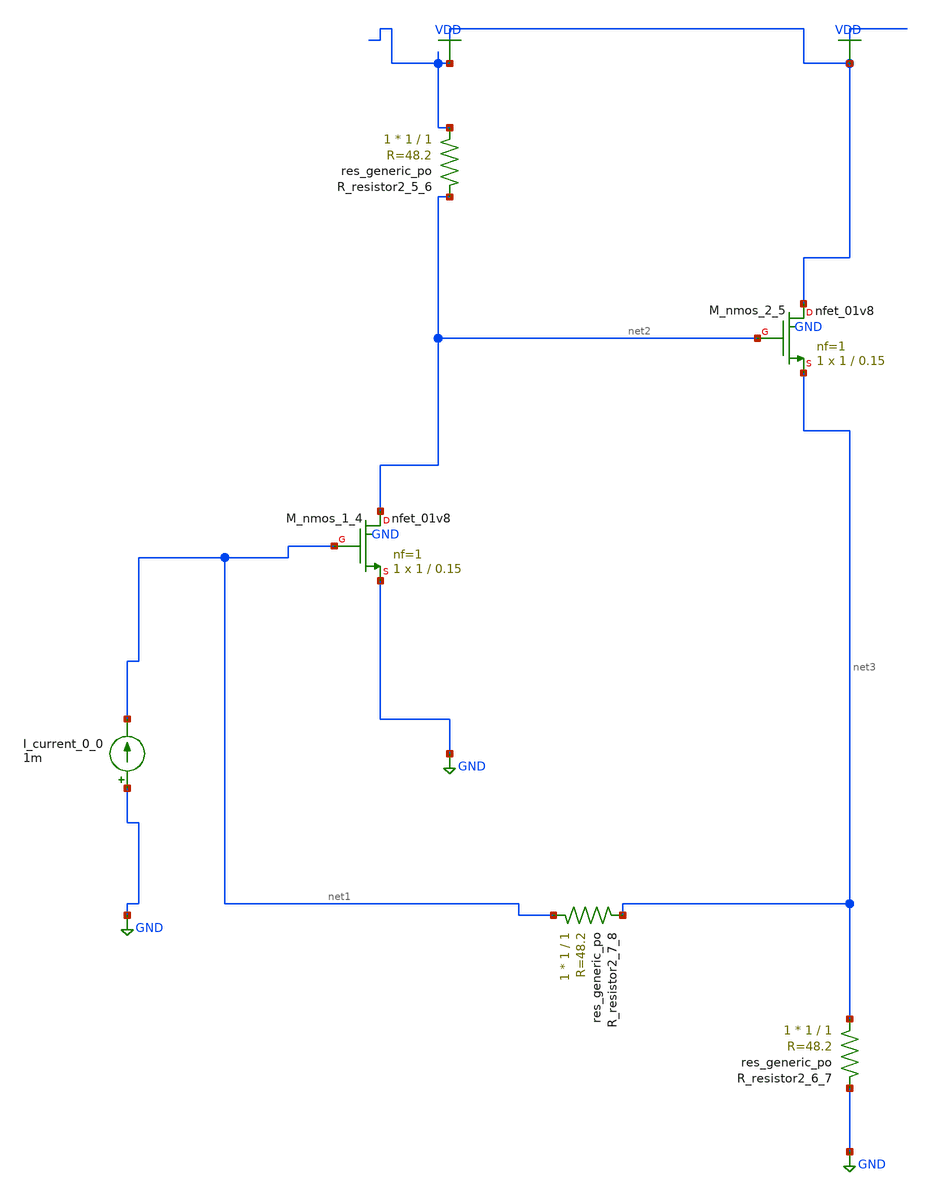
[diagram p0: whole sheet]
** sch_path: schematics/AMSNet/583.sch
**.subckt 583
I_current_0_0 GND net1 1m
XM_nmos_1_4 net2 net1 GND GND sky130_fd_pr__nfet_01v8 L=0.15 W=1 nf=1 ad='int((1 + 1)/2) * 1 / 1 * 0.29'
+ as='int((1 + 2)/2) * 1 / 1 * 0.29' pd='2*int((1 + 1)/2) * (1 / 1 + 0.29)' ps='2*int((1 + 2)/2) * (1 / 1 + 0.29)'
+ nrd='0.29 / 1 ' nrs='0.29 / 1 ' sa=0 sb=0 sd=0 mult=1 m=1
XM_nmos_2_5 VDD net2 net3 GND sky130_fd_pr__nfet_01v8 L=0.15 W=1 nf=1 ad='int((1 + 1)/2) * 1 / 1 * 0.29'
+ as='int((1 + 2)/2) * 1 / 1 * 0.29' pd='2*int((1 + 1)/2) * (1 / 1 + 0.29)' ps='2*int((1 + 2)/2) * (1 / 1 + 0.29)'
+ nrd='0.29 / 1 ' nrs='0.29 / 1 ' sa=0 sb=0 sd=0 mult=1 m=1
XR_resistor2_5_6 VDD net2 sky130_fd_pr__res_generic_po W=1 L=1 m=1
XR_resistor2_6_7 net3 GND sky130_fd_pr__res_generic_po W=1 L=1 m=1
XR_resistor2_7_8 net1 net3 sky130_fd_pr__res_generic_po W=1 L=1 m=1
**.ends
.GLOBAL GND
.GLOBAL VDD
.end
